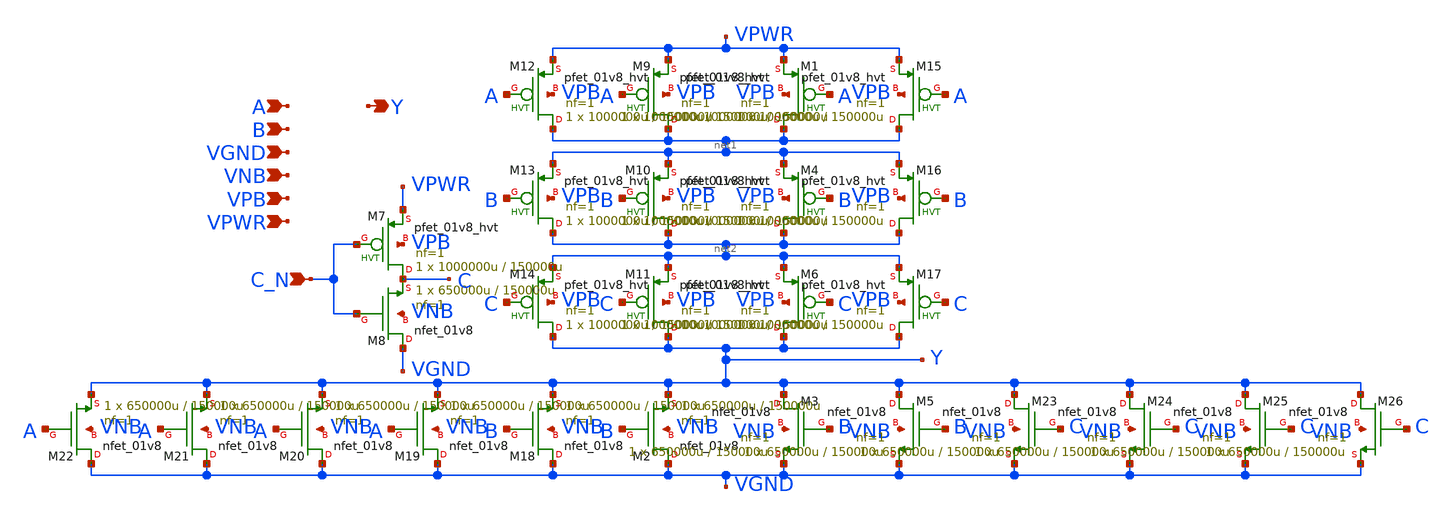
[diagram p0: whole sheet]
** sch_path: schematics/nor3b/sky130_fd_sc_hd__nor3b_4.sch
**.subckt sky130_fd_sc_hd__nor3b_4 A B C_N VGND VNB VPB VPWR Y
*.ipin A
*.ipin B
*.ipin C_N
*.ipin VGND
*.ipin VNB
*.ipin VPB
*.ipin VPWR
*.opin Y
XM1 net1 A VPWR VPB sky130_fd_pr__pfet_01v8_hvt L=150000u W=1000000u nf=1 ad='int((1 + 1)/2) * 1000000u / 1 * 0.29'
+ as='int((1 + 2)/2) * 1000000u / 1 * 0.29' pd='2*int((1 + 1)/2) * (1000000u / 1 + 0.29)' ps='2*int((1 + 2)/2) * (1000000u / 1 + 0.29)'
+ nrd='0.29 / 1000000u ' nrs='0.29 / 1000000u ' sa=0 sb=0 sd=0 mult=1 m=1
XM2 VGND B Y VNB sky130_fd_pr__nfet_01v8 L=150000u W=650000u nf=1 ad='int((1 + 1)/2) * 650000u / 1 * 0.29'
+ as='int((1 + 2)/2) * 650000u / 1 * 0.29' pd='2*int((1 + 1)/2) * (650000u / 1 + 0.29)' ps='2*int((1 + 2)/2) * (650000u / 1 + 0.29)'
+ nrd='0.29 / 650000u ' nrs='0.29 / 650000u ' sa=0 sb=0 sd=0 mult=1 m=1
XM4 net2 B net1 VPB sky130_fd_pr__pfet_01v8_hvt L=150000u W=1000000u nf=1 ad='int((1 + 1)/2) * 1000000u / 1 * 0.29'
+ as='int((1 + 2)/2) * 1000000u / 1 * 0.29' pd='2*int((1 + 1)/2) * (1000000u / 1 + 0.29)' ps='2*int((1 + 2)/2) * (1000000u / 1 + 0.29)'
+ nrd='0.29 / 1000000u ' nrs='0.29 / 1000000u ' sa=0 sb=0 sd=0 mult=1 m=1
XM6 Y C net2 VPB sky130_fd_pr__pfet_01v8_hvt L=150000u W=1000000u nf=1 ad='int((1 + 1)/2) * 1000000u / 1 * 0.29'
+ as='int((1 + 2)/2) * 1000000u / 1 * 0.29' pd='2*int((1 + 1)/2) * (1000000u / 1 + 0.29)' ps='2*int((1 + 2)/2) * (1000000u / 1 + 0.29)'
+ nrd='0.29 / 1000000u ' nrs='0.29 / 1000000u ' sa=0 sb=0 sd=0 mult=1 m=1
XM7 C C_N VPWR VPB sky130_fd_pr__pfet_01v8_hvt L=150000u W=1000000u nf=1 ad='int((1 + 1)/2) * 1000000u / 1 * 0.29'
+ as='int((1 + 2)/2) * 1000000u / 1 * 0.29' pd='2*int((1 + 1)/2) * (1000000u / 1 + 0.29)' ps='2*int((1 + 2)/2) * (1000000u / 1 + 0.29)'
+ nrd='0.29 / 1000000u ' nrs='0.29 / 1000000u ' sa=0 sb=0 sd=0 mult=1 m=1
XM8 VGND C_N C VNB sky130_fd_pr__nfet_01v8 L=150000u W=650000u nf=1 ad='int((1 + 1)/2) * 650000u / 1 * 0.29'
+ as='int((1 + 2)/2) * 650000u / 1 * 0.29' pd='2*int((1 + 1)/2) * (650000u / 1 + 0.29)' ps='2*int((1 + 2)/2) * (650000u / 1 + 0.29)'
+ nrd='0.29 / 650000u ' nrs='0.29 / 650000u ' sa=0 sb=0 sd=0 mult=1 m=1
XM5 Y B VGND VNB sky130_fd_pr__nfet_01v8 L=150000u W=650000u nf=1 ad='int((1 + 1)/2) * 650000u / 1 * 0.29'
+ as='int((1 + 2)/2) * 650000u / 1 * 0.29' pd='2*int((1 + 1)/2) * (650000u / 1 + 0.29)' ps='2*int((1 + 2)/2) * (650000u / 1 + 0.29)'
+ nrd='0.29 / 650000u ' nrs='0.29 / 650000u ' sa=0 sb=0 sd=0 mult=1 m=1
XM3 Y B VGND VNB sky130_fd_pr__nfet_01v8 L=150000u W=650000u nf=1 ad='int((1 + 1)/2) * 650000u / 1 * 0.29'
+ as='int((1 + 2)/2) * 650000u / 1 * 0.29' pd='2*int((1 + 1)/2) * (650000u / 1 + 0.29)' ps='2*int((1 + 2)/2) * (650000u / 1 + 0.29)'
+ nrd='0.29 / 650000u ' nrs='0.29 / 650000u ' sa=0 sb=0 sd=0 mult=1 m=1
XM9 net1 A VPWR VPB sky130_fd_pr__pfet_01v8_hvt L=150000u W=1000000u nf=1 ad='int((1 + 1)/2) * 1000000u / 1 * 0.29'
+ as='int((1 + 2)/2) * 1000000u / 1 * 0.29' pd='2*int((1 + 1)/2) * (1000000u / 1 + 0.29)' ps='2*int((1 + 2)/2) * (1000000u / 1 + 0.29)'
+ nrd='0.29 / 1000000u ' nrs='0.29 / 1000000u ' sa=0 sb=0 sd=0 mult=1 m=1
XM10 net2 B net1 VPB sky130_fd_pr__pfet_01v8_hvt L=150000u W=1000000u nf=1 ad='int((1 + 1)/2) * 1000000u / 1 * 0.29'
+ as='int((1 + 2)/2) * 1000000u / 1 * 0.29' pd='2*int((1 + 1)/2) * (1000000u / 1 + 0.29)' ps='2*int((1 + 2)/2) * (1000000u / 1 + 0.29)'
+ nrd='0.29 / 1000000u ' nrs='0.29 / 1000000u ' sa=0 sb=0 sd=0 mult=1 m=1
XM11 Y C net2 VPB sky130_fd_pr__pfet_01v8_hvt L=150000u W=1000000u nf=1 ad='int((1 + 1)/2) * 1000000u / 1 * 0.29'
+ as='int((1 + 2)/2) * 1000000u / 1 * 0.29' pd='2*int((1 + 1)/2) * (1000000u / 1 + 0.29)' ps='2*int((1 + 2)/2) * (1000000u / 1 + 0.29)'
+ nrd='0.29 / 1000000u ' nrs='0.29 / 1000000u ' sa=0 sb=0 sd=0 mult=1 m=1
XM12 net1 A VPWR VPB sky130_fd_pr__pfet_01v8_hvt L=150000u W=1000000u nf=1 ad='int((1 + 1)/2) * 1000000u / 1 * 0.29'
+ as='int((1 + 2)/2) * 1000000u / 1 * 0.29' pd='2*int((1 + 1)/2) * (1000000u / 1 + 0.29)' ps='2*int((1 + 2)/2) * (1000000u / 1 + 0.29)'
+ nrd='0.29 / 1000000u ' nrs='0.29 / 1000000u ' sa=0 sb=0 sd=0 mult=1 m=1
XM13 net2 B net1 VPB sky130_fd_pr__pfet_01v8_hvt L=150000u W=1000000u nf=1 ad='int((1 + 1)/2) * 1000000u / 1 * 0.29'
+ as='int((1 + 2)/2) * 1000000u / 1 * 0.29' pd='2*int((1 + 1)/2) * (1000000u / 1 + 0.29)' ps='2*int((1 + 2)/2) * (1000000u / 1 + 0.29)'
+ nrd='0.29 / 1000000u ' nrs='0.29 / 1000000u ' sa=0 sb=0 sd=0 mult=1 m=1
XM14 Y C net2 VPB sky130_fd_pr__pfet_01v8_hvt L=150000u W=1000000u nf=1 ad='int((1 + 1)/2) * 1000000u / 1 * 0.29'
+ as='int((1 + 2)/2) * 1000000u / 1 * 0.29' pd='2*int((1 + 1)/2) * (1000000u / 1 + 0.29)' ps='2*int((1 + 2)/2) * (1000000u / 1 + 0.29)'
+ nrd='0.29 / 1000000u ' nrs='0.29 / 1000000u ' sa=0 sb=0 sd=0 mult=1 m=1
XM15 net1 A VPWR VPB sky130_fd_pr__pfet_01v8_hvt L=150000u W=1000000u nf=1 ad='int((1 + 1)/2) * 1000000u / 1 * 0.29'
+ as='int((1 + 2)/2) * 1000000u / 1 * 0.29' pd='2*int((1 + 1)/2) * (1000000u / 1 + 0.29)' ps='2*int((1 + 2)/2) * (1000000u / 1 + 0.29)'
+ nrd='0.29 / 1000000u ' nrs='0.29 / 1000000u ' sa=0 sb=0 sd=0 mult=1 m=1
XM16 net2 B net1 VPB sky130_fd_pr__pfet_01v8_hvt L=150000u W=1000000u nf=1 ad='int((1 + 1)/2) * 1000000u / 1 * 0.29'
+ as='int((1 + 2)/2) * 1000000u / 1 * 0.29' pd='2*int((1 + 1)/2) * (1000000u / 1 + 0.29)' ps='2*int((1 + 2)/2) * (1000000u / 1 + 0.29)'
+ nrd='0.29 / 1000000u ' nrs='0.29 / 1000000u ' sa=0 sb=0 sd=0 mult=1 m=1
XM17 Y C net2 VPB sky130_fd_pr__pfet_01v8_hvt L=150000u W=1000000u nf=1 ad='int((1 + 1)/2) * 1000000u / 1 * 0.29'
+ as='int((1 + 2)/2) * 1000000u / 1 * 0.29' pd='2*int((1 + 1)/2) * (1000000u / 1 + 0.29)' ps='2*int((1 + 2)/2) * (1000000u / 1 + 0.29)'
+ nrd='0.29 / 1000000u ' nrs='0.29 / 1000000u ' sa=0 sb=0 sd=0 mult=1 m=1
XM18 VGND B Y VNB sky130_fd_pr__nfet_01v8 L=150000u W=650000u nf=1 ad='int((1 + 1)/2) * 650000u / 1 * 0.29'
+ as='int((1 + 2)/2) * 650000u / 1 * 0.29' pd='2*int((1 + 1)/2) * (650000u / 1 + 0.29)' ps='2*int((1 + 2)/2) * (650000u / 1 + 0.29)'
+ nrd='0.29 / 650000u ' nrs='0.29 / 650000u ' sa=0 sb=0 sd=0 mult=1 m=1
XM19 VGND A Y VNB sky130_fd_pr__nfet_01v8 L=150000u W=650000u nf=1 ad='int((1 + 1)/2) * 650000u / 1 * 0.29'
+ as='int((1 + 2)/2) * 650000u / 1 * 0.29' pd='2*int((1 + 1)/2) * (650000u / 1 + 0.29)' ps='2*int((1 + 2)/2) * (650000u / 1 + 0.29)'
+ nrd='0.29 / 650000u ' nrs='0.29 / 650000u ' sa=0 sb=0 sd=0 mult=1 m=1
XM20 VGND A Y VNB sky130_fd_pr__nfet_01v8 L=150000u W=650000u nf=1 ad='int((1 + 1)/2) * 650000u / 1 * 0.29'
+ as='int((1 + 2)/2) * 650000u / 1 * 0.29' pd='2*int((1 + 1)/2) * (650000u / 1 + 0.29)' ps='2*int((1 + 2)/2) * (650000u / 1 + 0.29)'
+ nrd='0.29 / 650000u ' nrs='0.29 / 650000u ' sa=0 sb=0 sd=0 mult=1 m=1
XM21 VGND A Y VNB sky130_fd_pr__nfet_01v8 L=150000u W=650000u nf=1 ad='int((1 + 1)/2) * 650000u / 1 * 0.29'
+ as='int((1 + 2)/2) * 650000u / 1 * 0.29' pd='2*int((1 + 1)/2) * (650000u / 1 + 0.29)' ps='2*int((1 + 2)/2) * (650000u / 1 + 0.29)'
+ nrd='0.29 / 650000u ' nrs='0.29 / 650000u ' sa=0 sb=0 sd=0 mult=1 m=1
XM22 VGND A Y VNB sky130_fd_pr__nfet_01v8 L=150000u W=650000u nf=1 ad='int((1 + 1)/2) * 650000u / 1 * 0.29'
+ as='int((1 + 2)/2) * 650000u / 1 * 0.29' pd='2*int((1 + 1)/2) * (650000u / 1 + 0.29)' ps='2*int((1 + 2)/2) * (650000u / 1 + 0.29)'
+ nrd='0.29 / 650000u ' nrs='0.29 / 650000u ' sa=0 sb=0 sd=0 mult=1 m=1
XM23 Y C VGND VNB sky130_fd_pr__nfet_01v8 L=150000u W=650000u nf=1 ad='int((1 + 1)/2) * 650000u / 1 * 0.29'
+ as='int((1 + 2)/2) * 650000u / 1 * 0.29' pd='2*int((1 + 1)/2) * (650000u / 1 + 0.29)' ps='2*int((1 + 2)/2) * (650000u / 1 + 0.29)'
+ nrd='0.29 / 650000u ' nrs='0.29 / 650000u ' sa=0 sb=0 sd=0 mult=1 m=1
XM24 Y C VGND VNB sky130_fd_pr__nfet_01v8 L=150000u W=650000u nf=1 ad='int((1 + 1)/2) * 650000u / 1 * 0.29'
+ as='int((1 + 2)/2) * 650000u / 1 * 0.29' pd='2*int((1 + 1)/2) * (650000u / 1 + 0.29)' ps='2*int((1 + 2)/2) * (650000u / 1 + 0.29)'
+ nrd='0.29 / 650000u ' nrs='0.29 / 650000u ' sa=0 sb=0 sd=0 mult=1 m=1
XM25 Y C VGND VNB sky130_fd_pr__nfet_01v8 L=150000u W=650000u nf=1 ad='int((1 + 1)/2) * 650000u / 1 * 0.29'
+ as='int((1 + 2)/2) * 650000u / 1 * 0.29' pd='2*int((1 + 1)/2) * (650000u / 1 + 0.29)' ps='2*int((1 + 2)/2) * (650000u / 1 + 0.29)'
+ nrd='0.29 / 650000u ' nrs='0.29 / 650000u ' sa=0 sb=0 sd=0 mult=1 m=1
XM26 Y C VGND VNB sky130_fd_pr__nfet_01v8 L=150000u W=650000u nf=1 ad='int((1 + 1)/2) * 650000u / 1 * 0.29'
+ as='int((1 + 2)/2) * 650000u / 1 * 0.29' pd='2*int((1 + 1)/2) * (650000u / 1 + 0.29)' ps='2*int((1 + 2)/2) * (650000u / 1 + 0.29)'
+ nrd='0.29 / 650000u ' nrs='0.29 / 650000u ' sa=0 sb=0 sd=0 mult=1 m=1
**.ends
.end
